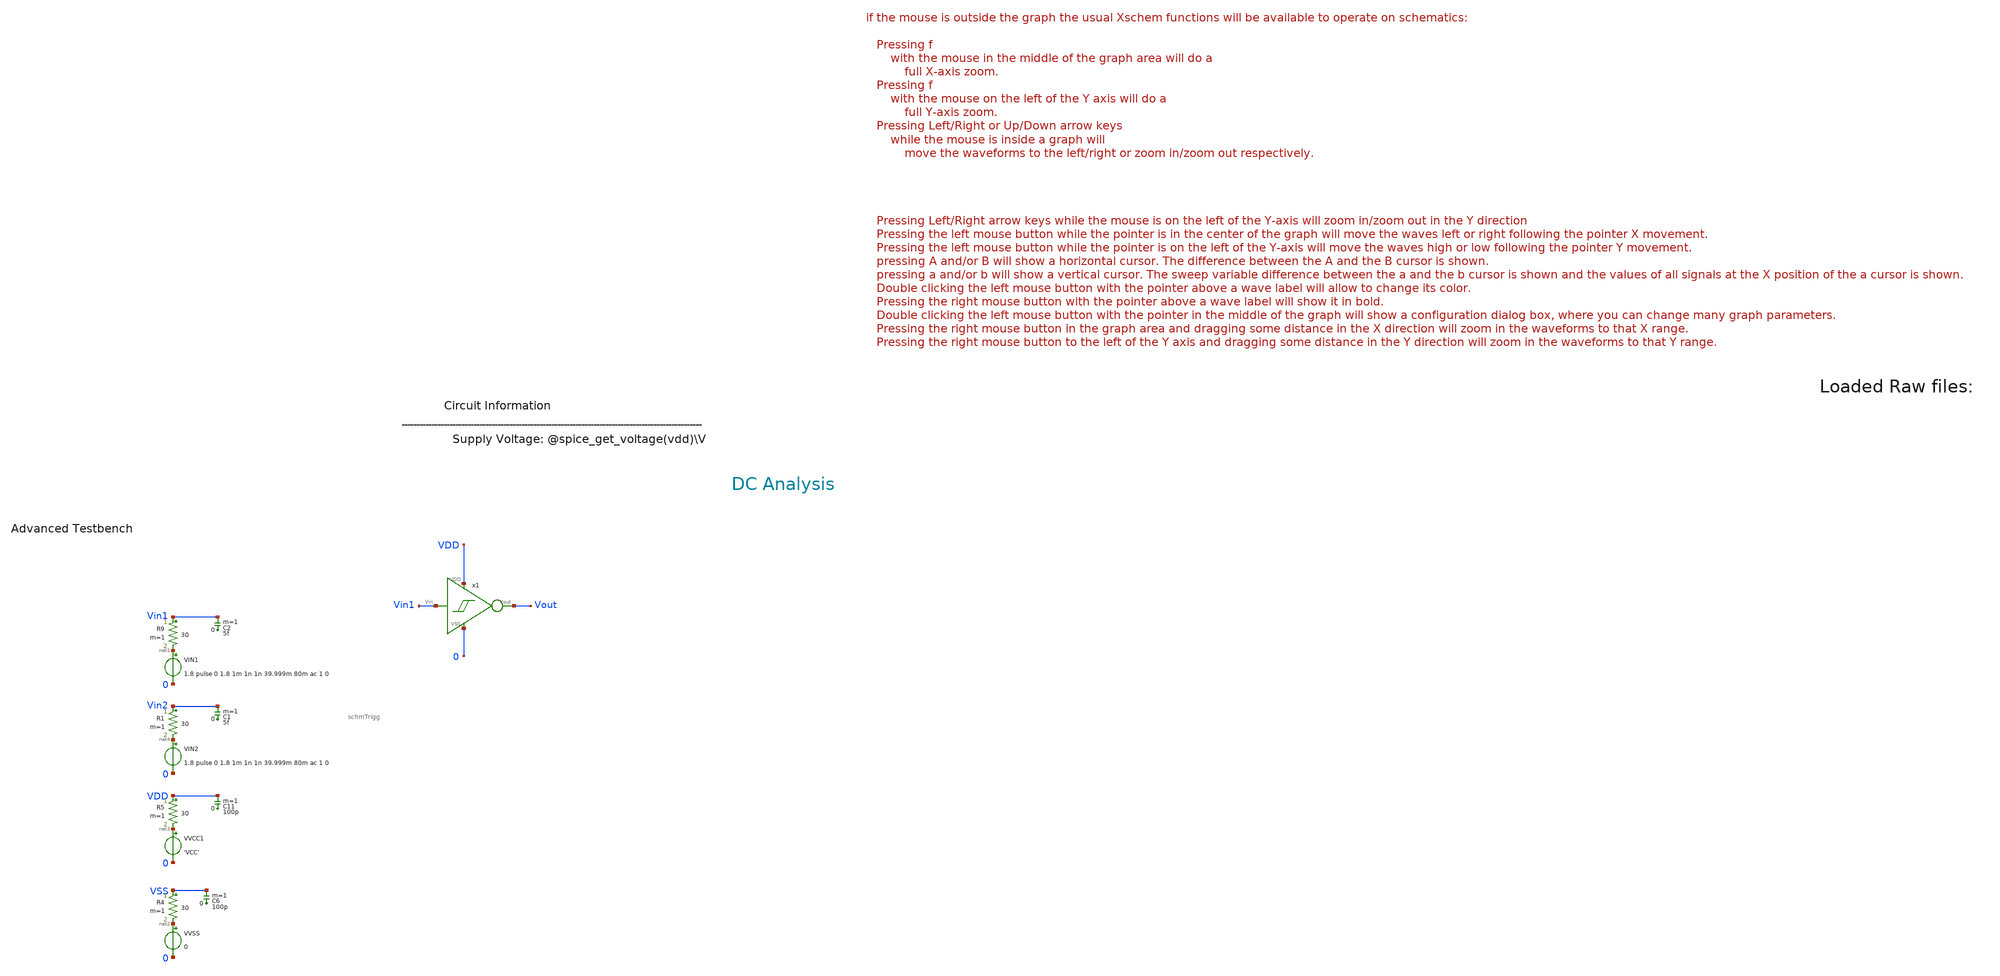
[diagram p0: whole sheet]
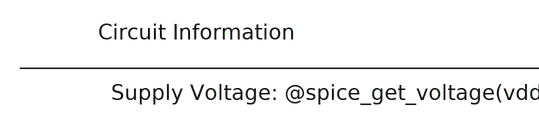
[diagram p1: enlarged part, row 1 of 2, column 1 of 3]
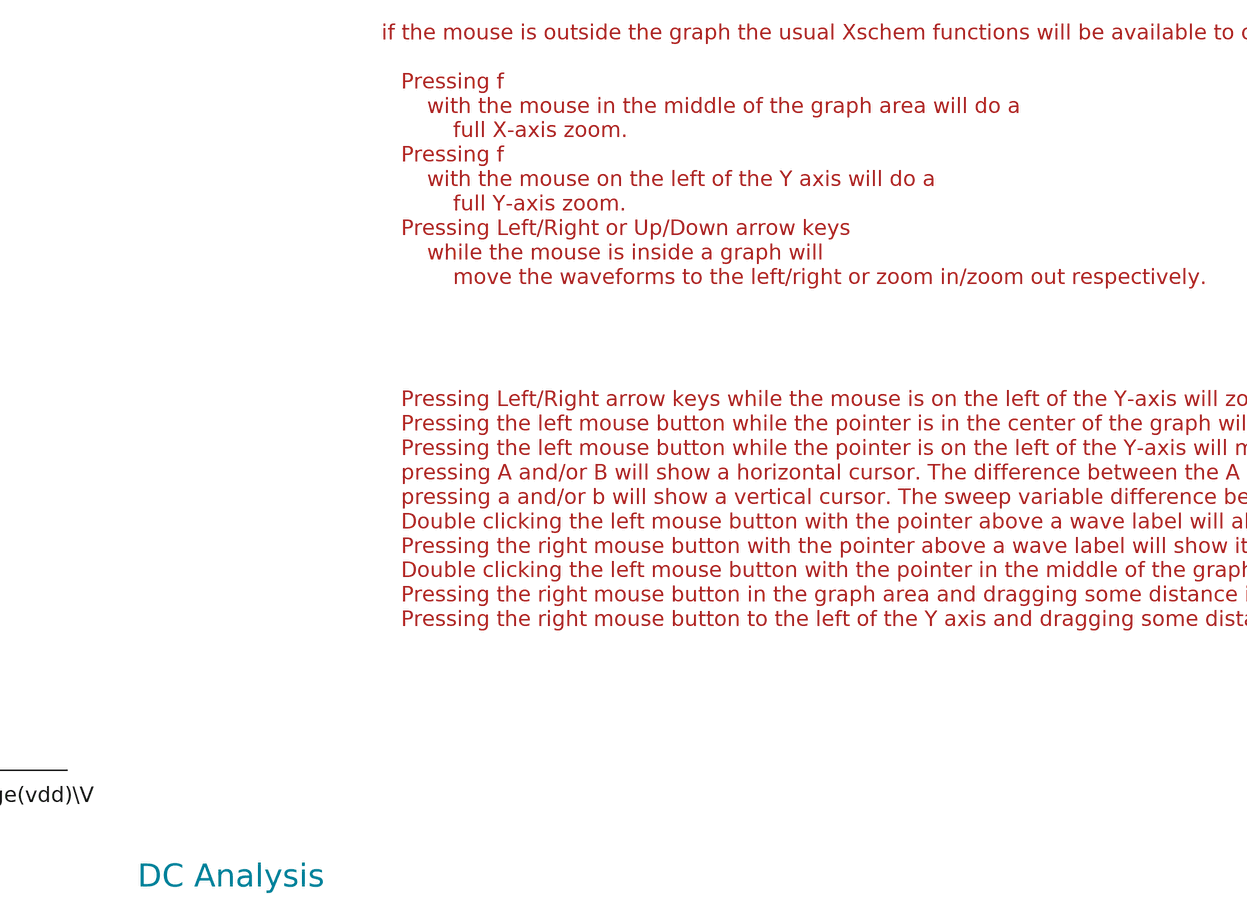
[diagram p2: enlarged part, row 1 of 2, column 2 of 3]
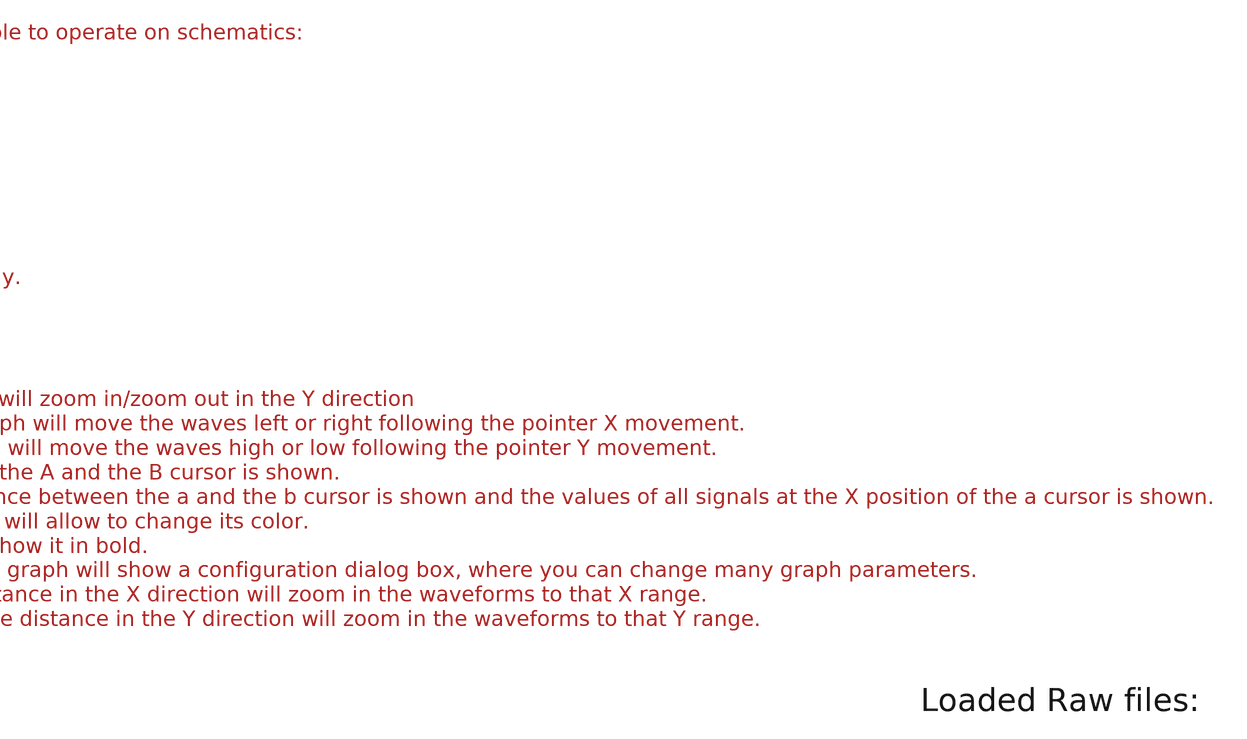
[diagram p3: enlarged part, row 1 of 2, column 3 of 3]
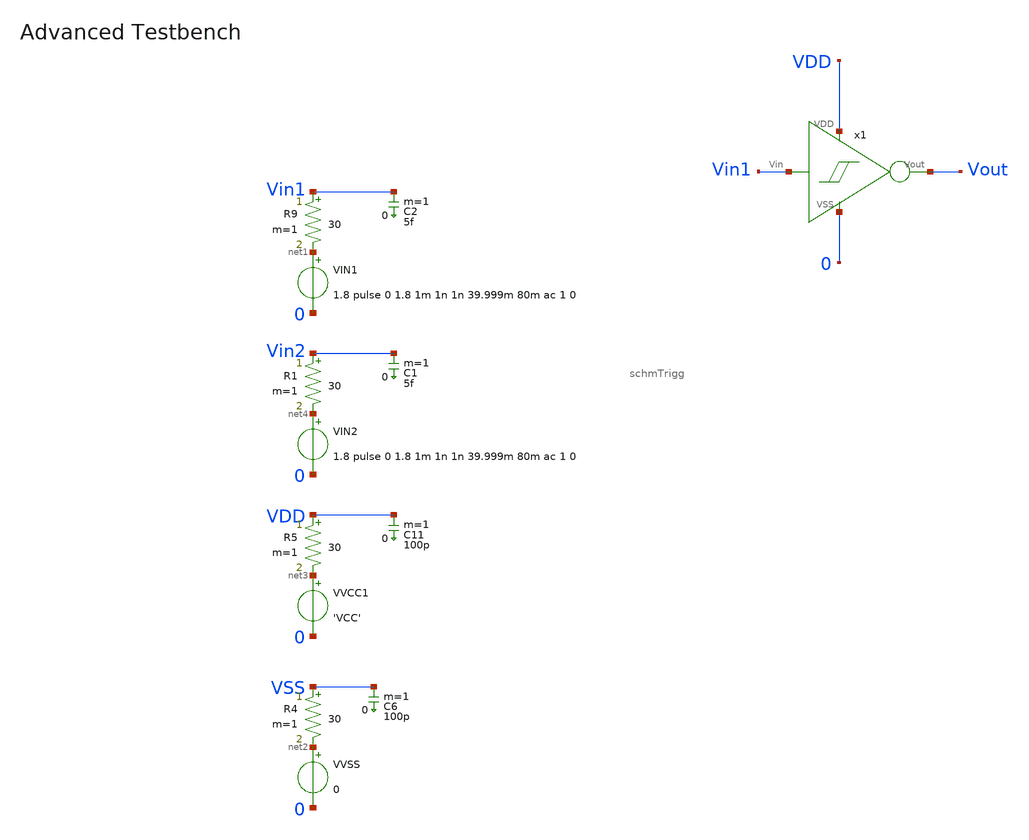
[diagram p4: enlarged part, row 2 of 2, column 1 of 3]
** sch_path: xschem/T1/schmTrigg/schmTrigg_tb.sch
* Copyright (C) 1998-2024 Stefan Frederik Schippers
* This program is free software; you can redistribute it and/or modify
* it under the terms of the GNU General Public License as published by
* the Free Software Foundation; either version 2 of the License, or
* (at your option) any later version.
* This program is distributed in the hope that it will be useful,
* but WITHOUT ANY WARRANTY; without even the implied warranty of
* MERCHANTABILITY or FITNESS FOR A PARTICULAR PURPOSE.  See the
* GNU General Public License for more details.
* You should have received a copy of the GNU General Public License
* along with this program; if not, write to the Free Software
**.subckt schmTrigg_tb
VIN1 net1 0 1.8 pulse 0 1.8 1m 1n 1n 39.999m 80m ac 1 0
VVSS net2 0 0
R4 VSS net2 30 m=1
C6 VSS 0 100p m=1
VVCC1 net3 0 'VCC'
R5 VDD net3 30 m=1
C11 VDD 0 100p m=1
R9 Vin1 net1 30 m=1
C2 Vin1 0 5f m=1
x1 Vin1 0 VDD Vout schmTrigg
VIN2 net4 0 1.8 pulse 0 1.8 1m 1n 1n 39.999m 80m ac 1 0
R1 Vin2 net4 30 m=1
C1 Vin2 0 5f m=1
**** begin user architecture code



.temp 30
*.param IB=1n
.param VCC = 1.8

.option savecurrents
.save all @m1[gm]
.control
  save all alli
  op
  let power=-v(vcc) * i(vvcc)
  settype power power
  write template_adv_tb.raw
  set appendwrite



  dc vin1 0 1.8 0.005
  write template_adv_tb.raw

  tran 1u 2m
  *tran 0.01n 15n
  write template_adv_tb.raw

  *ac dec 10 1 1G
  *remzerovec
  *write template_adv_tb.raw



  quit 0




.endc





** opencircuitdesign pdks install
.lib $::SKYWATER_MODELS/sky130.lib.spice tt
.include $::SKYWATER_STDCELLS/sky130_fd_sc_hd.spice


**** end user architecture code
**.ends

* expanding   symbol:  T1/schmTrigg/schmTrigg.sym # of pins=4
** sym_path: xschem/T1/schmTrigg/schmTrigg.sym
** sch_path: xschem/T1/schmTrigg/schmTrigg.sch
.subckt schmTrigg Vin VSS VDD Vout
*.ipin Vin
*.ipin VDD
*.ipin VSS
*.opin Vout
XM1 VDD Vout Vn Vn sky130_fd_pr__nfet_01v8 L=0.15 W=1 nf=1 ad='int((1 + 1)/2) * 1 / 1 * 0.29' as='int((1 + 2)/2) * 1 / 1 * 0.29'
+ pd='2*int((1 + 1)/2) * (1 / 1 + 0.29)' ps='2*int((1 + 2)/2) * (1 / 1 + 0.29)' nrd='0.29 / 1 ' nrs='0.29 / 1 '
+ sa=0 sb=0 sd=0 mult=1 m=1
XM2 Vn Vin VSS VSS sky130_fd_pr__nfet_01v8 L=0.15 W=1 nf=1 ad='int((1 + 1)/2) * 1 / 1 * 0.29' as='int((1 + 2)/2) * 1 / 1 * 0.29'
+ pd='2*int((1 + 1)/2) * (1 / 1 + 0.29)' ps='2*int((1 + 2)/2) * (1 / 1 + 0.29)' nrd='0.29 / 1 ' nrs='0.29 / 1 '
+ sa=0 sb=0 sd=0 mult=1 m=1
XM3 Vout Vin Vn Vn sky130_fd_pr__nfet_01v8 L=0.15 W=1 nf=1 ad='int((1 + 1)/2) * 1 / 1 * 0.29' as='int((1 + 2)/2) * 1 / 1 * 0.29'
+ pd='2*int((1 + 1)/2) * (1 / 1 + 0.29)' ps='2*int((1 + 2)/2) * (1 / 1 + 0.29)' nrd='0.29 / 1 ' nrs='0.29 / 1 '
+ sa=0 sb=0 sd=0 mult=1 m=1
XM4 VSS Vout Vp Vp sky130_fd_pr__pfet_01v8 L=0.15 W=1 nf=1 ad='int((nf+1)/2) * W/nf * 0.29' as='int((nf+2)/2) * W/nf * 0.29'
+ pd='2*int((nf+1)/2) * (W/nf + 0.29)' ps='2*int((nf+2)/2) * (W/nf + 0.29)' nrd='0.29 / W' nrs='0.29 / W'
+ sa=0 sb=0 sd=0 mult=1 m=1
XM5 Vout Vin Vp Vp sky130_fd_pr__pfet_01v8 L=0.15 W=1 nf=1 ad='int((nf+1)/2) * W/nf * 0.29' as='int((nf+2)/2) * W/nf * 0.29'
+ pd='2*int((nf+1)/2) * (W/nf + 0.29)' ps='2*int((nf+2)/2) * (W/nf + 0.29)' nrd='0.29 / W' nrs='0.29 / W'
+ sa=0 sb=0 sd=0 mult=1 m=1
XM6 Vp Vin VDD VDD sky130_fd_pr__pfet_01v8 L=0.15 W=1 nf=1 ad='int((nf+1)/2) * W/nf * 0.29' as='int((nf+2)/2) * W/nf * 0.29'
+ pd='2*int((nf+1)/2) * (W/nf + 0.29)' ps='2*int((nf+2)/2) * (W/nf + 0.29)' nrd='0.29 / W' nrs='0.29 / W'
+ sa=0 sb=0 sd=0 mult=1 m=1
.ends

.end
